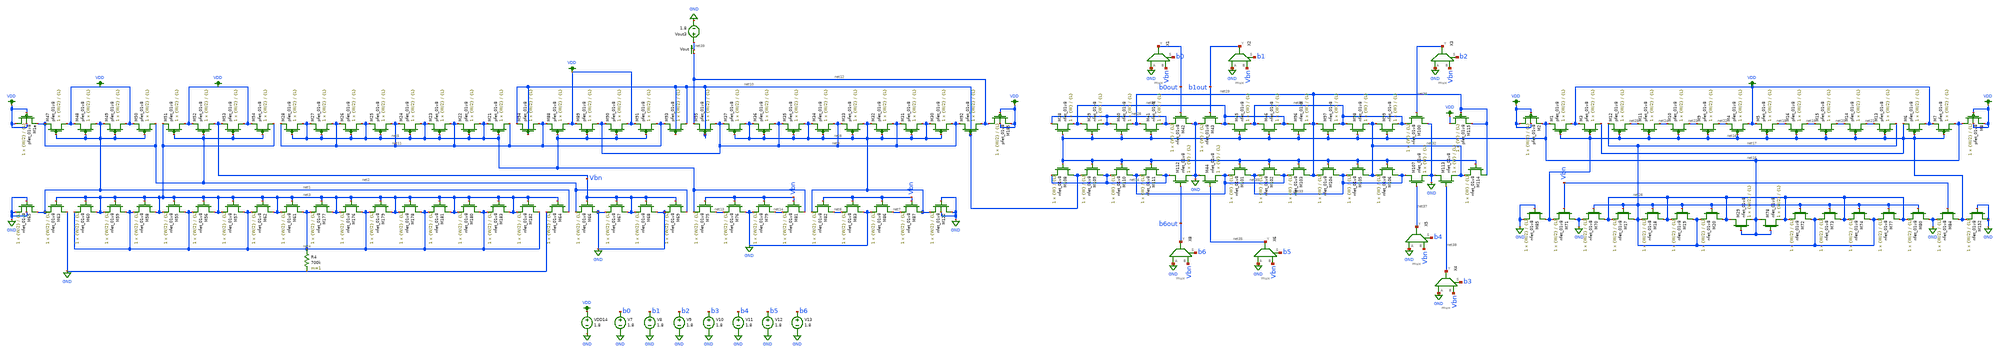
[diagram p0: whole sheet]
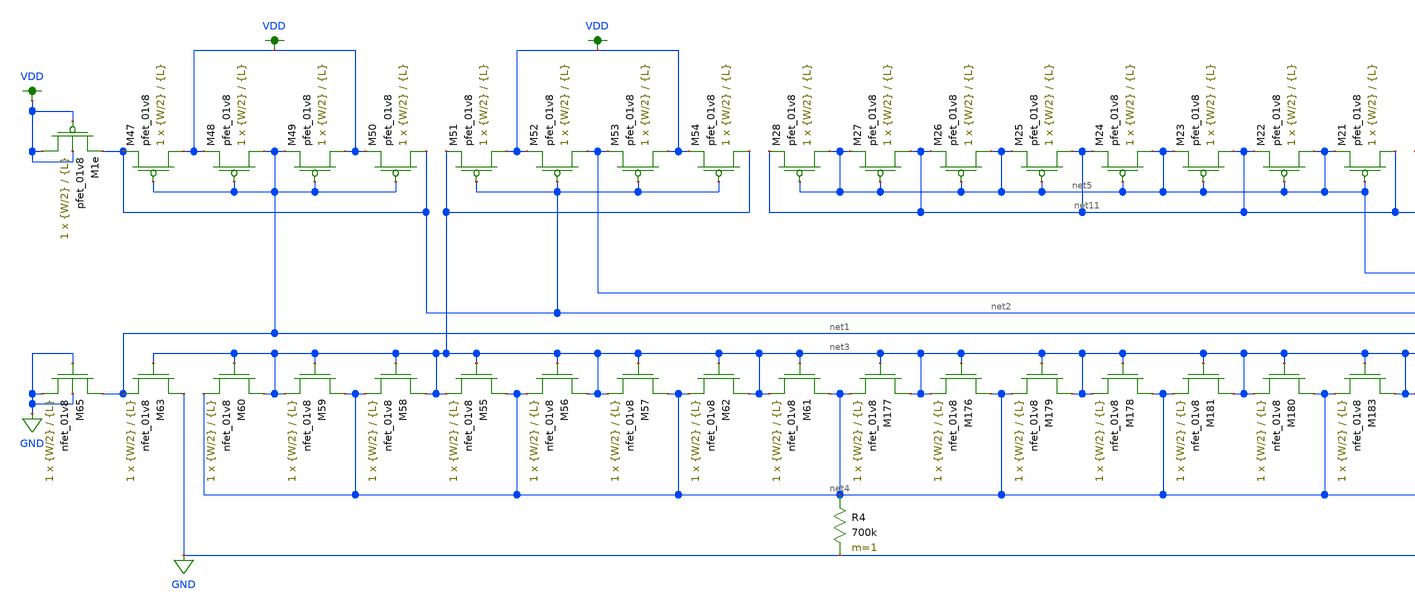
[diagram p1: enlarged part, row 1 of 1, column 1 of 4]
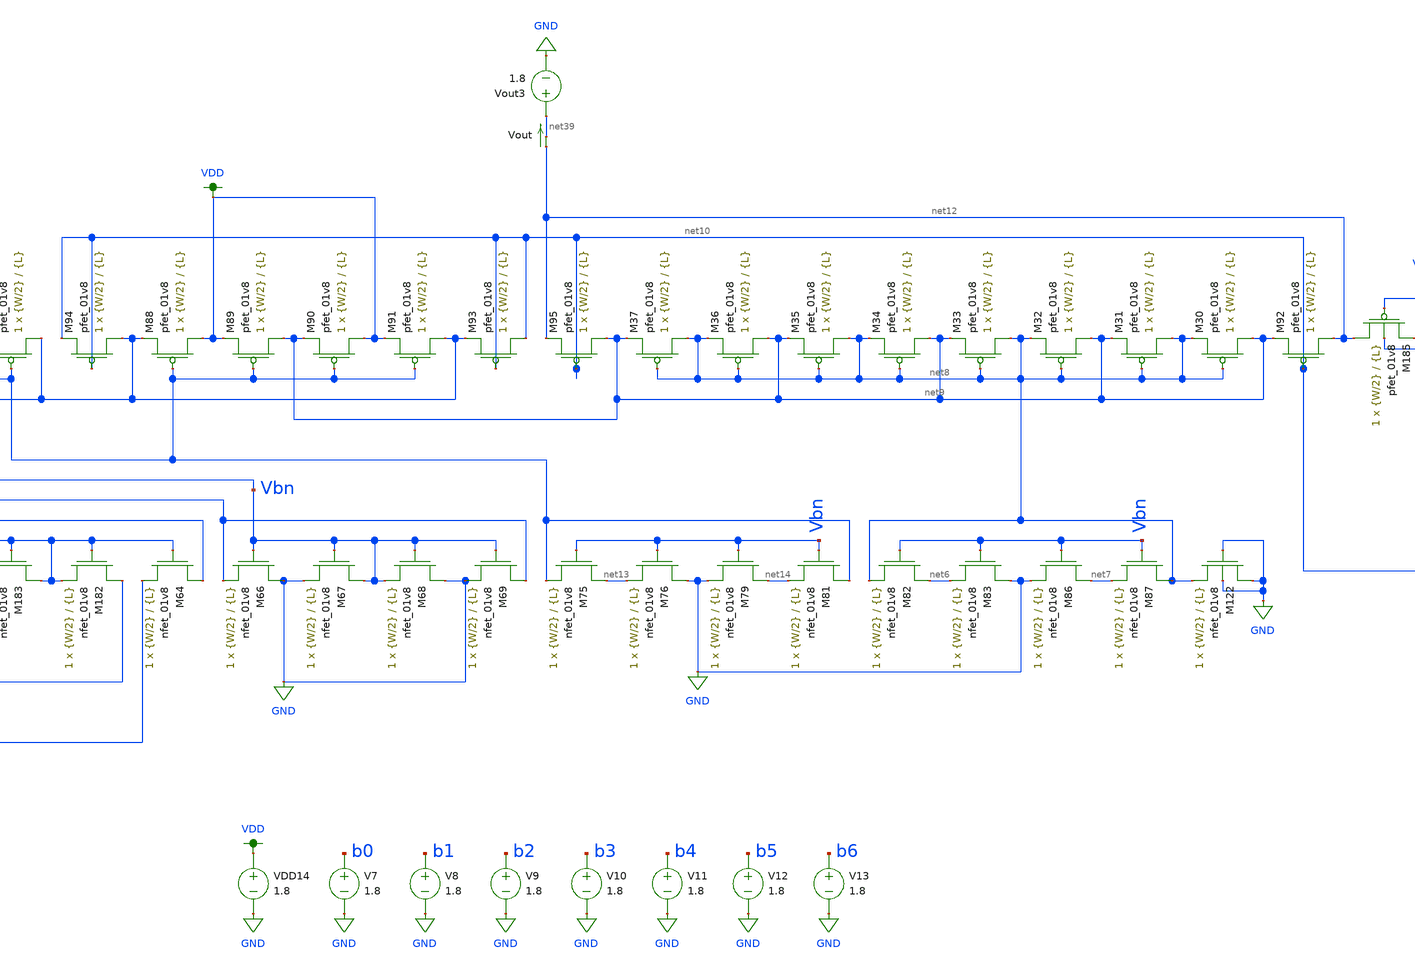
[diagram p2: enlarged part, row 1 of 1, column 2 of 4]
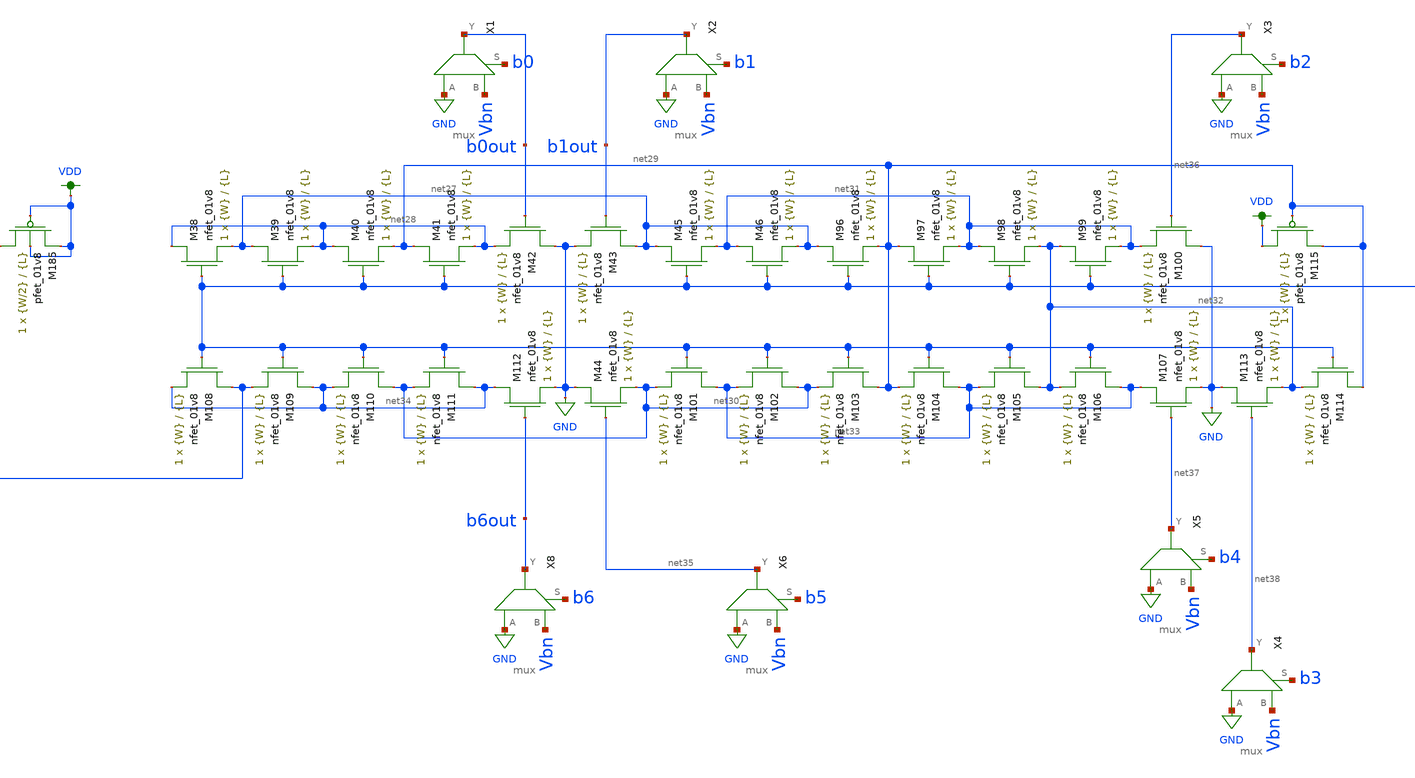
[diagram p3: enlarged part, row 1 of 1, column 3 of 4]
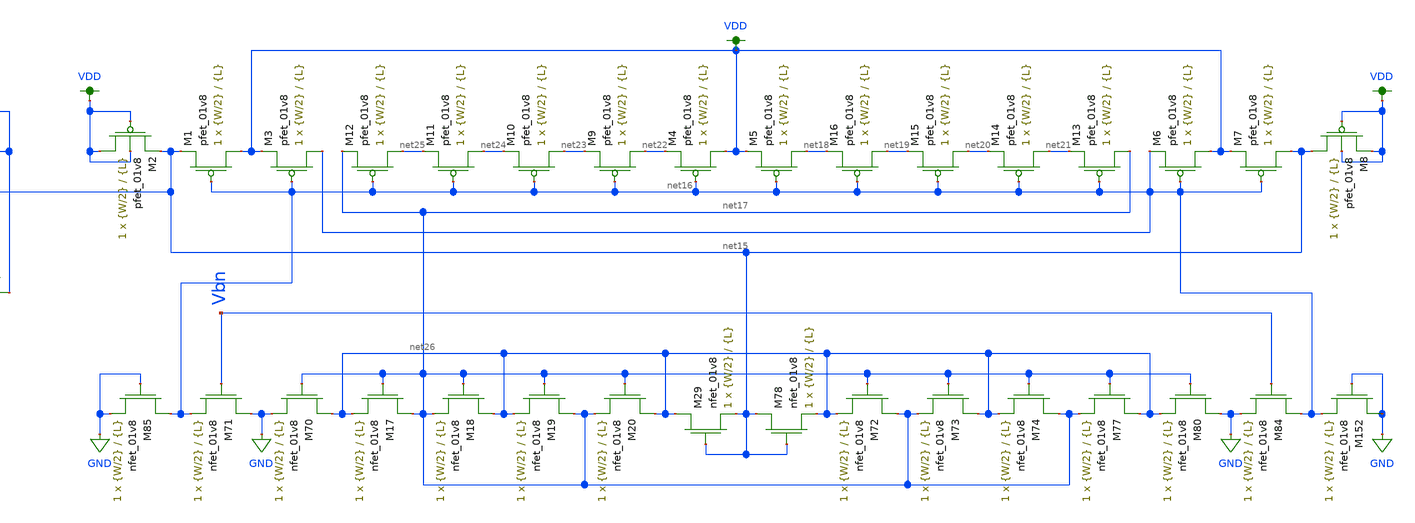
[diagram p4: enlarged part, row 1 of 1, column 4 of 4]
** sch_path: dac/schematics/dac_voltage_current_current_mirror_lds.sch
**.subckt dac_voltage_current_current_mirror_lds
XM47 VDD net1 net2 VDD sky130_fd_pr__pfet_01v8 L={L} W={W/2} nf=1 ad='int((nf+1)/2) * W/nf * 0.29' as='int((nf+2)/2) * W/nf * 0.29'
+ pd='2*int((nf+1)/2) * (W/nf + 0.29)' ps='2*int((nf+2)/2) * (W/nf + 0.29)' nrd='0.29 / W' nrs='0.29 / W'
+ sa=0 sb=0 sd=0 mult=1 m=1
XM48 net1 net1 VDD VDD sky130_fd_pr__pfet_01v8 L={L} W={W/2} nf=1 ad='int((nf+1)/2) * W/nf * 0.29' as='int((nf+2)/2) * W/nf * 0.29'
+ pd='2*int((nf+1)/2) * (W/nf + 0.29)' ps='2*int((nf+2)/2) * (W/nf + 0.29)' nrd='0.29 / W' nrs='0.29 / W'
+ sa=0 sb=0 sd=0 mult=1 m=1
XM49 VDD net1 net1 VDD sky130_fd_pr__pfet_01v8 L={L} W={W/2} nf=1 ad='int((nf+1)/2) * W/nf * 0.29' as='int((nf+2)/2) * W/nf * 0.29'
+ pd='2*int((nf+1)/2) * (W/nf + 0.29)' ps='2*int((nf+2)/2) * (W/nf + 0.29)' nrd='0.29 / W' nrs='0.29 / W'
+ sa=0 sb=0 sd=0 mult=1 m=1
XM50 net2 net1 VDD VDD sky130_fd_pr__pfet_01v8 L={L} W={W/2} nf=1 ad='int((nf+1)/2) * W/nf * 0.29' as='int((nf+2)/2) * W/nf * 0.29'
+ pd='2*int((nf+1)/2) * (W/nf + 0.29)' ps='2*int((nf+2)/2) * (W/nf + 0.29)' nrd='0.29 / W' nrs='0.29 / W'
+ sa=0 sb=0 sd=0 mult=1 m=1
XM51 VDD net2 net3 VDD sky130_fd_pr__pfet_01v8 L={L} W={W/2} nf=1 ad='int((nf+1)/2) * W/nf * 0.29' as='int((nf+2)/2) * W/nf * 0.29'
+ pd='2*int((nf+1)/2) * (W/nf + 0.29)' ps='2*int((nf+2)/2) * (W/nf + 0.29)' nrd='0.29 / W' nrs='0.29 / W'
+ sa=0 sb=0 sd=0 mult=1 m=1
XM52 Vbn net2 VDD VDD sky130_fd_pr__pfet_01v8 L={L} W={W/2} nf=1 ad='int((nf+1)/2) * W/nf * 0.29' as='int((nf+2)/2) * W/nf * 0.29'
+ pd='2*int((nf+1)/2) * (W/nf + 0.29)' ps='2*int((nf+2)/2) * (W/nf + 0.29)' nrd='0.29 / W' nrs='0.29 / W'
+ sa=0 sb=0 sd=0 mult=1 m=1
XM53 VDD net2 Vbn VDD sky130_fd_pr__pfet_01v8 L={L} W={W/2} nf=1 ad='int((nf+1)/2) * W/nf * 0.29' as='int((nf+2)/2) * W/nf * 0.29'
+ pd='2*int((nf+1)/2) * (W/nf + 0.29)' ps='2*int((nf+2)/2) * (W/nf + 0.29)' nrd='0.29 / W' nrs='0.29 / W'
+ sa=0 sb=0 sd=0 mult=1 m=1
XM54 net3 net2 VDD VDD sky130_fd_pr__pfet_01v8 L={L} W={W/2} nf=1 ad='int((nf+1)/2) * W/nf * 0.29' as='int((nf+2)/2) * W/nf * 0.29'
+ pd='2*int((nf+1)/2) * (W/nf + 0.29)' ps='2*int((nf+2)/2) * (W/nf + 0.29)' nrd='0.29 / W' nrs='0.29 / W'
+ sa=0 sb=0 sd=0 mult=1 m=1
XM55 net4 net3 net3 GND sky130_fd_pr__nfet_01v8 L={L} W={W/2} nf=1 ad='int((nf+1)/2) * W/nf * 0.29' as='int((nf+2)/2) * W/nf * 0.29'
+ pd='2*int((nf+1)/2) * (W/nf + 0.29)' ps='2*int((nf+2)/2) * (W/nf + 0.29)' nrd='0.29 / W' nrs='0.29 / W'
+ sa=0 sb=0 sd=0 mult=1 m=1
XM56 net3 net3 net4 GND sky130_fd_pr__nfet_01v8 L={L} W={W/2} nf=1 ad='int((nf+1)/2) * W/nf * 0.29' as='int((nf+2)/2) * W/nf * 0.29'
+ pd='2*int((nf+1)/2) * (W/nf + 0.29)' ps='2*int((nf+2)/2) * (W/nf + 0.29)' nrd='0.29 / W' nrs='0.29 / W'
+ sa=0 sb=0 sd=0 mult=1 m=1
XM57 net4 net3 net3 GND sky130_fd_pr__nfet_01v8 L={L} W={W/2} nf=1 ad='int((nf+1)/2) * W/nf * 0.29' as='int((nf+2)/2) * W/nf * 0.29'
+ pd='2*int((nf+1)/2) * (W/nf + 0.29)' ps='2*int((nf+2)/2) * (W/nf + 0.29)' nrd='0.29 / W' nrs='0.29 / W'
+ sa=0 sb=0 sd=0 mult=1 m=1
XM58 net3 net3 net4 GND sky130_fd_pr__nfet_01v8 L={L} W={W/2} nf=1 ad='int((nf+1)/2) * W/nf * 0.29' as='int((nf+2)/2) * W/nf * 0.29'
+ pd='2*int((nf+1)/2) * (W/nf + 0.29)' ps='2*int((nf+2)/2) * (W/nf + 0.29)' nrd='0.29 / W' nrs='0.29 / W'
+ sa=0 sb=0 sd=0 mult=1 m=1
XM59 net4 net3 net3 GND sky130_fd_pr__nfet_01v8 L={L} W={W/2} nf=1 ad='int((nf+1)/2) * W/nf * 0.29' as='int((nf+2)/2) * W/nf * 0.29'
+ pd='2*int((nf+1)/2) * (W/nf + 0.29)' ps='2*int((nf+2)/2) * (W/nf + 0.29)' nrd='0.29 / W' nrs='0.29 / W'
+ sa=0 sb=0 sd=0 mult=1 m=1
XM60 net3 net3 net4 GND sky130_fd_pr__nfet_01v8 L={L} W={W/2} nf=1 ad='int((nf+1)/2) * W/nf * 0.29' as='int((nf+2)/2) * W/nf * 0.29'
+ pd='2*int((nf+1)/2) * (W/nf + 0.29)' ps='2*int((nf+2)/2) * (W/nf + 0.29)' nrd='0.29 / W' nrs='0.29 / W'
+ sa=0 sb=0 sd=0 mult=1 m=1
XM61 net4 net3 net3 GND sky130_fd_pr__nfet_01v8 L={L} W={W/2} nf=1 ad='int((nf+1)/2) * W/nf * 0.29' as='int((nf+2)/2) * W/nf * 0.29'
+ pd='2*int((nf+1)/2) * (W/nf + 0.29)' ps='2*int((nf+2)/2) * (W/nf + 0.29)' nrd='0.29 / W' nrs='0.29 / W'
+ sa=0 sb=0 sd=0 mult=1 m=1
XM62 net3 net3 net4 GND sky130_fd_pr__nfet_01v8 L={L} W={W/2} nf=1 ad='int((nf+1)/2) * W/nf * 0.29' as='int((nf+2)/2) * W/nf * 0.29'
+ pd='2*int((nf+1)/2) * (W/nf + 0.29)' ps='2*int((nf+2)/2) * (W/nf + 0.29)' nrd='0.29 / W' nrs='0.29 / W'
+ sa=0 sb=0 sd=0 mult=1 m=1
XM63 GND net3 net1 GND sky130_fd_pr__nfet_01v8 L={L} W={W/2} nf=1 ad='int((nf+1)/2) * W/nf * 0.29' as='int((nf+2)/2) * W/nf * 0.29'
+ pd='2*int((nf+1)/2) * (W/nf + 0.29)' ps='2*int((nf+2)/2) * (W/nf + 0.29)' nrd='0.29 / W' nrs='0.29 / W'
+ sa=0 sb=0 sd=0 mult=1 m=1
XM64 net1 net3 GND GND sky130_fd_pr__nfet_01v8 L={L} W={W/2} nf=1 ad='int((nf+1)/2) * W/nf * 0.29' as='int((nf+2)/2) * W/nf * 0.29'
+ pd='2*int((nf+1)/2) * (W/nf + 0.29)' ps='2*int((nf+2)/2) * (W/nf + 0.29)' nrd='0.29 / W' nrs='0.29 / W'
+ sa=0 sb=0 sd=0 mult=1 m=1
R4 net4 GND 700k m=1
XM1e VDD VDD net2 VDD sky130_fd_pr__pfet_01v8 L={L} W={W/2} nf=1 ad='int((nf+1)/2) * W/nf * 0.29' as='int((nf+2)/2) * W/nf * 0.29'
+ pd='2*int((nf+1)/2) * (W/nf + 0.29)' ps='2*int((nf+2)/2) * (W/nf + 0.29)' nrd='0.29 / W' nrs='0.29 / W'
+ sa=0 sb=0 sd=0 mult=1 m=1
XM65 net1 GND GND GND sky130_fd_pr__nfet_01v8 L={L} W={W/2} nf=1 ad='int((nf+1)/2) * W/nf * 0.29' as='int((nf+2)/2) * W/nf * 0.29'
+ pd='2*int((nf+1)/2) * (W/nf + 0.29)' ps='2*int((nf+2)/2) * (W/nf + 0.29)' nrd='0.29 / W' nrs='0.29 / W'
+ sa=0 sb=0 sd=0 mult=1 m=1
XM66 GND Vbn net2 GND sky130_fd_pr__nfet_01v8 L={L} W={W/2} nf=1 ad='int((nf+1)/2) * W/nf * 0.29' as='int((nf+2)/2) * W/nf * 0.29'
+ pd='2*int((nf+1)/2) * (W/nf + 0.29)' ps='2*int((nf+2)/2) * (W/nf + 0.29)' nrd='0.29 / W' nrs='0.29 / W'
+ sa=0 sb=0 sd=0 mult=1 m=1
XM67 Vbn Vbn GND GND sky130_fd_pr__nfet_01v8 L={L} W={W/2} nf=1 ad='int((nf+1)/2) * W/nf * 0.29' as='int((nf+2)/2) * W/nf * 0.29'
+ pd='2*int((nf+1)/2) * (W/nf + 0.29)' ps='2*int((nf+2)/2) * (W/nf + 0.29)' nrd='0.29 / W' nrs='0.29 / W'
+ sa=0 sb=0 sd=0 mult=1 m=1
XM68 GND Vbn Vbn GND sky130_fd_pr__nfet_01v8 L={L} W={W/2} nf=1 ad='int((nf+1)/2) * W/nf * 0.29' as='int((nf+2)/2) * W/nf * 0.29'
+ pd='2*int((nf+1)/2) * (W/nf + 0.29)' ps='2*int((nf+2)/2) * (W/nf + 0.29)' nrd='0.29 / W' nrs='0.29 / W'
+ sa=0 sb=0 sd=0 mult=1 m=1
XM69 net2 Vbn GND GND sky130_fd_pr__nfet_01v8 L={L} W={W/2} nf=1 ad='int((nf+1)/2) * W/nf * 0.29' as='int((nf+2)/2) * W/nf * 0.29'
+ pd='2*int((nf+1)/2) * (W/nf + 0.29)' ps='2*int((nf+2)/2) * (W/nf + 0.29)' nrd='0.29 / W' nrs='0.29 / W'
+ sa=0 sb=0 sd=0 mult=1 m=1
XM75 net13 Vbn net5 GND sky130_fd_pr__nfet_01v8 L={L} W={W/2} nf=1 ad='int((nf+1)/2) * W/nf * 0.29' as='int((nf+2)/2) * W/nf * 0.29'
+ pd='2*int((nf+1)/2) * (W/nf + 0.29)' ps='2*int((nf+2)/2) * (W/nf + 0.29)' nrd='0.29 / W' nrs='0.29 / W'
+ sa=0 sb=0 sd=0 mult=1 m=1
XM76 GND Vbn net13 GND sky130_fd_pr__nfet_01v8 L={L} W={W/2} nf=1 ad='int((nf+1)/2) * W/nf * 0.29' as='int((nf+2)/2) * W/nf * 0.29'
+ pd='2*int((nf+1)/2) * (W/nf + 0.29)' ps='2*int((nf+2)/2) * (W/nf + 0.29)' nrd='0.29 / W' nrs='0.29 / W'
+ sa=0 sb=0 sd=0 mult=1 m=1
XM79 net14 Vbn GND GND sky130_fd_pr__nfet_01v8 L={L} W={W/2} nf=1 ad='int((nf+1)/2) * W/nf * 0.29' as='int((nf+2)/2) * W/nf * 0.29'
+ pd='2*int((nf+1)/2) * (W/nf + 0.29)' ps='2*int((nf+2)/2) * (W/nf + 0.29)' nrd='0.29 / W' nrs='0.29 / W'
+ sa=0 sb=0 sd=0 mult=1 m=1
XM81 net5 Vbn net14 GND sky130_fd_pr__nfet_01v8 L={L} W={W/2} nf=1 ad='int((nf+1)/2) * W/nf * 0.29' as='int((nf+2)/2) * W/nf * 0.29'
+ pd='2*int((nf+1)/2) * (W/nf + 0.29)' ps='2*int((nf+2)/2) * (W/nf + 0.29)' nrd='0.29 / W' nrs='0.29 / W'
+ sa=0 sb=0 sd=0 mult=1 m=1
XM82 net6 Vbn net8 GND sky130_fd_pr__nfet_01v8 L={L} W={W/2} nf=1 ad='int((nf+1)/2) * W/nf * 0.29' as='int((nf+2)/2) * W/nf * 0.29'
+ pd='2*int((nf+1)/2) * (W/nf + 0.29)' ps='2*int((nf+2)/2) * (W/nf + 0.29)' nrd='0.29 / W' nrs='0.29 / W'
+ sa=0 sb=0 sd=0 mult=1 m=1
XM83 GND Vbn net6 GND sky130_fd_pr__nfet_01v8 L={L} W={W/2} nf=1 ad='int((nf+1)/2) * W/nf * 0.29' as='int((nf+2)/2) * W/nf * 0.29'
+ pd='2*int((nf+1)/2) * (W/nf + 0.29)' ps='2*int((nf+2)/2) * (W/nf + 0.29)' nrd='0.29 / W' nrs='0.29 / W'
+ sa=0 sb=0 sd=0 mult=1 m=1
XM86 net7 Vbn GND GND sky130_fd_pr__nfet_01v8 L={L} W={W/2} nf=1 ad='int((nf+1)/2) * W/nf * 0.29' as='int((nf+2)/2) * W/nf * 0.29'
+ pd='2*int((nf+1)/2) * (W/nf + 0.29)' ps='2*int((nf+2)/2) * (W/nf + 0.29)' nrd='0.29 / W' nrs='0.29 / W'
+ sa=0 sb=0 sd=0 mult=1 m=1
XM87 net8 Vbn net7 GND sky130_fd_pr__nfet_01v8 L={L} W={W/2} nf=1 ad='int((nf+1)/2) * W/nf * 0.29' as='int((nf+2)/2) * W/nf * 0.29'
+ pd='2*int((nf+1)/2) * (W/nf + 0.29)' ps='2*int((nf+2)/2) * (W/nf + 0.29)' nrd='0.29 / W' nrs='0.29 / W'
+ sa=0 sb=0 sd=0 mult=1 m=1
XM88 VDD net5 net11 VDD sky130_fd_pr__pfet_01v8 L={L} W={W/2} nf=1 ad='int((nf+1)/2) * W/nf * 0.29' as='int((nf+2)/2) * W/nf * 0.29'
+ pd='2*int((nf+1)/2) * (W/nf + 0.29)' ps='2*int((nf+2)/2) * (W/nf + 0.29)' nrd='0.29 / W' nrs='0.29 / W'
+ sa=0 sb=0 sd=0 mult=1 m=1
XM89 net9 net5 VDD VDD sky130_fd_pr__pfet_01v8 L={L} W={W/2} nf=1 ad='int((nf+1)/2) * W/nf * 0.29' as='int((nf+2)/2) * W/nf * 0.29'
+ pd='2*int((nf+1)/2) * (W/nf + 0.29)' ps='2*int((nf+2)/2) * (W/nf + 0.29)' nrd='0.29 / W' nrs='0.29 / W'
+ sa=0 sb=0 sd=0 mult=1 m=1
XM90 VDD net5 net9 VDD sky130_fd_pr__pfet_01v8 L={L} W={W/2} nf=1 ad='int((nf+1)/2) * W/nf * 0.29' as='int((nf+2)/2) * W/nf * 0.29'
+ pd='2*int((nf+1)/2) * (W/nf + 0.29)' ps='2*int((nf+2)/2) * (W/nf + 0.29)' nrd='0.29 / W' nrs='0.29 / W'
+ sa=0 sb=0 sd=0 mult=1 m=1
XM91 net11 net5 VDD VDD sky130_fd_pr__pfet_01v8 L={L} W={W/2} nf=1 ad='int((nf+1)/2) * W/nf * 0.29' as='int((nf+2)/2) * W/nf * 0.29'
+ pd='2*int((nf+1)/2) * (W/nf + 0.29)' ps='2*int((nf+2)/2) * (W/nf + 0.29)' nrd='0.29 / W' nrs='0.29 / W'
+ sa=0 sb=0 sd=0 mult=1 m=1
XM92 net12 net10 net9 VDD sky130_fd_pr__pfet_01v8 L={L} W={W/2} nf=1 ad='int((nf+1)/2) * W/nf * 0.29'
+ as='int((nf+2)/2) * W/nf * 0.29' pd='2*int((nf+1)/2) * (W/nf + 0.29)' ps='2*int((nf+2)/2) * (W/nf + 0.29)'
+ nrd='0.29 / W' nrs='0.29 / W' sa=0 sb=0 sd=0 mult=1 m=1
XM93 net10 net10 net11 VDD sky130_fd_pr__pfet_01v8 L={L} W={W/2} nf=1 ad='int((nf+1)/2) * W/nf * 0.29'
+ as='int((nf+2)/2) * W/nf * 0.29' pd='2*int((nf+1)/2) * (W/nf + 0.29)' ps='2*int((nf+2)/2) * (W/nf + 0.29)'
+ nrd='0.29 / W' nrs='0.29 / W' sa=0 sb=0 sd=0 mult=1 m=1
XM94 net11 net10 net10 VDD sky130_fd_pr__pfet_01v8 L={L} W={W/2} nf=1 ad='int((nf+1)/2) * W/nf * 0.29'
+ as='int((nf+2)/2) * W/nf * 0.29' pd='2*int((nf+1)/2) * (W/nf + 0.29)' ps='2*int((nf+2)/2) * (W/nf + 0.29)'
+ nrd='0.29 / W' nrs='0.29 / W' sa=0 sb=0 sd=0 mult=1 m=1
XM95 net9 net10 net12 VDD sky130_fd_pr__pfet_01v8 L={L} W={W/2} nf=1 ad='int((nf+1)/2) * W/nf * 0.29'
+ as='int((nf+2)/2) * W/nf * 0.29' pd='2*int((nf+1)/2) * (W/nf + 0.29)' ps='2*int((nf+2)/2) * (W/nf + 0.29)'
+ nrd='0.29 / W' nrs='0.29 / W' sa=0 sb=0 sd=0 mult=1 m=1
XM176 net4 net3 net3 GND sky130_fd_pr__nfet_01v8 L={L} W={W/2} nf=1 ad='int((nf+1)/2) * W/nf * 0.29'
+ as='int((nf+2)/2) * W/nf * 0.29' pd='2*int((nf+1)/2) * (W/nf + 0.29)' ps='2*int((nf+2)/2) * (W/nf + 0.29)'
+ nrd='0.29 / W' nrs='0.29 / W' sa=0 sb=0 sd=0 mult=1 m=1
XM177 net3 net3 net4 GND sky130_fd_pr__nfet_01v8 L={L} W={W/2} nf=1 ad='int((nf+1)/2) * W/nf * 0.29'
+ as='int((nf+2)/2) * W/nf * 0.29' pd='2*int((nf+1)/2) * (W/nf + 0.29)' ps='2*int((nf+2)/2) * (W/nf + 0.29)'
+ nrd='0.29 / W' nrs='0.29 / W' sa=0 sb=0 sd=0 mult=1 m=1
XM178 net4 net3 net3 GND sky130_fd_pr__nfet_01v8 L={L} W={W/2} nf=1 ad='int((nf+1)/2) * W/nf * 0.29'
+ as='int((nf+2)/2) * W/nf * 0.29' pd='2*int((nf+1)/2) * (W/nf + 0.29)' ps='2*int((nf+2)/2) * (W/nf + 0.29)'
+ nrd='0.29 / W' nrs='0.29 / W' sa=0 sb=0 sd=0 mult=1 m=1
XM179 net3 net3 net4 GND sky130_fd_pr__nfet_01v8 L={L} W={W/2} nf=1 ad='int((nf+1)/2) * W/nf * 0.29'
+ as='int((nf+2)/2) * W/nf * 0.29' pd='2*int((nf+1)/2) * (W/nf + 0.29)' ps='2*int((nf+2)/2) * (W/nf + 0.29)'
+ nrd='0.29 / W' nrs='0.29 / W' sa=0 sb=0 sd=0 mult=1 m=1
XM180 net4 net3 net3 GND sky130_fd_pr__nfet_01v8 L={L} W={W/2} nf=1 ad='int((nf+1)/2) * W/nf * 0.29'
+ as='int((nf+2)/2) * W/nf * 0.29' pd='2*int((nf+1)/2) * (W/nf + 0.29)' ps='2*int((nf+2)/2) * (W/nf + 0.29)'
+ nrd='0.29 / W' nrs='0.29 / W' sa=0 sb=0 sd=0 mult=1 m=1
XM181 net3 net3 net4 GND sky130_fd_pr__nfet_01v8 L={L} W={W/2} nf=1 ad='int((nf+1)/2) * W/nf * 0.29'
+ as='int((nf+2)/2) * W/nf * 0.29' pd='2*int((nf+1)/2) * (W/nf + 0.29)' ps='2*int((nf+2)/2) * (W/nf + 0.29)'
+ nrd='0.29 / W' nrs='0.29 / W' sa=0 sb=0 sd=0 mult=1 m=1
XM182 net4 net3 net3 GND sky130_fd_pr__nfet_01v8 L={L} W={W/2} nf=1 ad='int((nf+1)/2) * W/nf * 0.29'
+ as='int((nf+2)/2) * W/nf * 0.29' pd='2*int((nf+1)/2) * (W/nf + 0.29)' ps='2*int((nf+2)/2) * (W/nf + 0.29)'
+ nrd='0.29 / W' nrs='0.29 / W' sa=0 sb=0 sd=0 mult=1 m=1
XM183 net3 net3 net4 GND sky130_fd_pr__nfet_01v8 L={L} W={W/2} nf=1 ad='int((nf+1)/2) * W/nf * 0.29'
+ as='int((nf+2)/2) * W/nf * 0.29' pd='2*int((nf+1)/2) * (W/nf + 0.29)' ps='2*int((nf+2)/2) * (W/nf + 0.29)'
+ nrd='0.29 / W' nrs='0.29 / W' sa=0 sb=0 sd=0 mult=1 m=1
XM185 net12 VDD VDD VDD sky130_fd_pr__pfet_01v8 L={L} W={W/2} nf=1 ad='int((nf+1)/2) * W/nf * 0.29' as='int((nf+2)/2) * W/nf * 0.29'
+ pd='2*int((nf+1)/2) * (W/nf + 0.29)' ps='2*int((nf+2)/2) * (W/nf + 0.29)' nrd='0.29 / W' nrs='0.29 / W'
+ sa=0 sb=0 sd=0 mult=1 m=1
Vout net12 net39 0
.save i(vout)
XM21 net11 net5 net5 VDD sky130_fd_pr__pfet_01v8 L={L} W={W/2} nf=1 ad='int((nf+1)/2) * W/nf * 0.29'
+ as='int((nf+2)/2) * W/nf * 0.29' pd='2*int((nf+1)/2) * (W/nf + 0.29)' ps='2*int((nf+2)/2) * (W/nf + 0.29)'
+ nrd='0.29 / W' nrs='0.29 / W' sa=0 sb=0 sd=0 mult=1 m=1
XM22 net5 net5 net11 VDD sky130_fd_pr__pfet_01v8 L={L} W={W/2} nf=1 ad='int((nf+1)/2) * W/nf * 0.29'
+ as='int((nf+2)/2) * W/nf * 0.29' pd='2*int((nf+1)/2) * (W/nf + 0.29)' ps='2*int((nf+2)/2) * (W/nf + 0.29)'
+ nrd='0.29 / W' nrs='0.29 / W' sa=0 sb=0 sd=0 mult=1 m=1
XM23 net11 net5 net5 VDD sky130_fd_pr__pfet_01v8 L={L} W={W/2} nf=1 ad='int((nf+1)/2) * W/nf * 0.29'
+ as='int((nf+2)/2) * W/nf * 0.29' pd='2*int((nf+1)/2) * (W/nf + 0.29)' ps='2*int((nf+2)/2) * (W/nf + 0.29)'
+ nrd='0.29 / W' nrs='0.29 / W' sa=0 sb=0 sd=0 mult=1 m=1
XM24 net5 net5 net11 VDD sky130_fd_pr__pfet_01v8 L={L} W={W/2} nf=1 ad='int((nf+1)/2) * W/nf * 0.29'
+ as='int((nf+2)/2) * W/nf * 0.29' pd='2*int((nf+1)/2) * (W/nf + 0.29)' ps='2*int((nf+2)/2) * (W/nf + 0.29)'
+ nrd='0.29 / W' nrs='0.29 / W' sa=0 sb=0 sd=0 mult=1 m=1
XM25 net11 net5 net5 VDD sky130_fd_pr__pfet_01v8 L={L} W={W/2} nf=1 ad='int((nf+1)/2) * W/nf * 0.29'
+ as='int((nf+2)/2) * W/nf * 0.29' pd='2*int((nf+1)/2) * (W/nf + 0.29)' ps='2*int((nf+2)/2) * (W/nf + 0.29)'
+ nrd='0.29 / W' nrs='0.29 / W' sa=0 sb=0 sd=0 mult=1 m=1
XM26 net5 net5 net11 VDD sky130_fd_pr__pfet_01v8 L={L} W={W/2} nf=1 ad='int((nf+1)/2) * W/nf * 0.29'
+ as='int((nf+2)/2) * W/nf * 0.29' pd='2*int((nf+1)/2) * (W/nf + 0.29)' ps='2*int((nf+2)/2) * (W/nf + 0.29)'
+ nrd='0.29 / W' nrs='0.29 / W' sa=0 sb=0 sd=0 mult=1 m=1
XM27 net11 net5 net5 VDD sky130_fd_pr__pfet_01v8 L={L} W={W/2} nf=1 ad='int((nf+1)/2) * W/nf * 0.29'
+ as='int((nf+2)/2) * W/nf * 0.29' pd='2*int((nf+1)/2) * (W/nf + 0.29)' ps='2*int((nf+2)/2) * (W/nf + 0.29)'
+ nrd='0.29 / W' nrs='0.29 / W' sa=0 sb=0 sd=0 mult=1 m=1
XM28 net5 net5 net11 VDD sky130_fd_pr__pfet_01v8 L={L} W={W/2} nf=1 ad='int((nf+1)/2) * W/nf * 0.29'
+ as='int((nf+2)/2) * W/nf * 0.29' pd='2*int((nf+1)/2) * (W/nf + 0.29)' ps='2*int((nf+2)/2) * (W/nf + 0.29)'
+ nrd='0.29 / W' nrs='0.29 / W' sa=0 sb=0 sd=0 mult=1 m=1
XM30 net9 net8 net8 VDD sky130_fd_pr__pfet_01v8 L={L} W={W/2} nf=1 ad='int((nf+1)/2) * W/nf * 0.29' as='int((nf+2)/2) * W/nf * 0.29'
+ pd='2*int((nf+1)/2) * (W/nf + 0.29)' ps='2*int((nf+2)/2) * (W/nf + 0.29)' nrd='0.29 / W' nrs='0.29 / W'
+ sa=0 sb=0 sd=0 mult=1 m=1
XM31 net8 net8 net9 VDD sky130_fd_pr__pfet_01v8 L={L} W={W/2} nf=1 ad='int((nf+1)/2) * W/nf * 0.29' as='int((nf+2)/2) * W/nf * 0.29'
+ pd='2*int((nf+1)/2) * (W/nf + 0.29)' ps='2*int((nf+2)/2) * (W/nf + 0.29)' nrd='0.29 / W' nrs='0.29 / W'
+ sa=0 sb=0 sd=0 mult=1 m=1
XM32 net9 net8 net8 VDD sky130_fd_pr__pfet_01v8 L={L} W={W/2} nf=1 ad='int((nf+1)/2) * W/nf * 0.29' as='int((nf+2)/2) * W/nf * 0.29'
+ pd='2*int((nf+1)/2) * (W/nf + 0.29)' ps='2*int((nf+2)/2) * (W/nf + 0.29)' nrd='0.29 / W' nrs='0.29 / W'
+ sa=0 sb=0 sd=0 mult=1 m=1
XM33 net8 net8 net9 VDD sky130_fd_pr__pfet_01v8 L={L} W={W/2} nf=1 ad='int((nf+1)/2) * W/nf * 0.29' as='int((nf+2)/2) * W/nf * 0.29'
+ pd='2*int((nf+1)/2) * (W/nf + 0.29)' ps='2*int((nf+2)/2) * (W/nf + 0.29)' nrd='0.29 / W' nrs='0.29 / W'
+ sa=0 sb=0 sd=0 mult=1 m=1
XM34 net9 net8 net8 VDD sky130_fd_pr__pfet_01v8 L={L} W={W/2} nf=1 ad='int((nf+1)/2) * W/nf * 0.29' as='int((nf+2)/2) * W/nf * 0.29'
+ pd='2*int((nf+1)/2) * (W/nf + 0.29)' ps='2*int((nf+2)/2) * (W/nf + 0.29)' nrd='0.29 / W' nrs='0.29 / W'
+ sa=0 sb=0 sd=0 mult=1 m=1
XM35 net8 net8 net9 VDD sky130_fd_pr__pfet_01v8 L={L} W={W/2} nf=1 ad='int((nf+1)/2) * W/nf * 0.29' as='int((nf+2)/2) * W/nf * 0.29'
+ pd='2*int((nf+1)/2) * (W/nf + 0.29)' ps='2*int((nf+2)/2) * (W/nf + 0.29)' nrd='0.29 / W' nrs='0.29 / W'
+ sa=0 sb=0 sd=0 mult=1 m=1
XM36 net9 net8 net8 VDD sky130_fd_pr__pfet_01v8 L={L} W={W/2} nf=1 ad='int((nf+1)/2) * W/nf * 0.29' as='int((nf+2)/2) * W/nf * 0.29'
+ pd='2*int((nf+1)/2) * (W/nf + 0.29)' ps='2*int((nf+2)/2) * (W/nf + 0.29)' nrd='0.29 / W' nrs='0.29 / W'
+ sa=0 sb=0 sd=0 mult=1 m=1
XM37 net8 net8 net9 VDD sky130_fd_pr__pfet_01v8 L={L} W={W/2} nf=1 ad='int((nf+1)/2) * W/nf * 0.29' as='int((nf+2)/2) * W/nf * 0.29'
+ pd='2*int((nf+1)/2) * (W/nf + 0.29)' ps='2*int((nf+2)/2) * (W/nf + 0.29)' nrd='0.29 / W' nrs='0.29 / W'
+ sa=0 sb=0 sd=0 mult=1 m=1
XM122 GND GND net8 GND sky130_fd_pr__nfet_01v8 L={L} W={W/2} nf=1 ad='int((nf+1)/2) * W/nf * 0.29' as='int((nf+2)/2) * W/nf * 0.29'
+ pd='2*int((nf+1)/2) * (W/nf + 0.29)' ps='2*int((nf+2)/2) * (W/nf + 0.29)' nrd='0.29 / W' nrs='0.29 / W'
+ sa=0 sb=0 sd=0 mult=1 m=1
XM1 VDD net16 net15 VDD sky130_fd_pr__pfet_01v8 L={L} W={W/2} nf=1 ad='int((nf+1)/2) * W/nf * 0.29' as='int((nf+2)/2) * W/nf * 0.29'
+ pd='2*int((nf+1)/2) * (W/nf + 0.29)' ps='2*int((nf+2)/2) * (W/nf + 0.29)' nrd='0.29 / W' nrs='0.29 / W'
+ sa=0 sb=0 sd=0 mult=1 m=1
XM2 VDD VDD net15 VDD sky130_fd_pr__pfet_01v8 L={L} W={W/2} nf=1 ad='int((nf+1)/2) * W/nf * 0.29' as='int((nf+2)/2) * W/nf * 0.29'
+ pd='2*int((nf+1)/2) * (W/nf + 0.29)' ps='2*int((nf+2)/2) * (W/nf + 0.29)' nrd='0.29 / W' nrs='0.29 / W'
+ sa=0 sb=0 sd=0 mult=1 m=1
XM3 net16 net16 VDD VDD sky130_fd_pr__pfet_01v8 L={L} W={W/2} nf=1 ad='int((nf+1)/2) * W/nf * 0.29' as='int((nf+2)/2) * W/nf * 0.29'
+ pd='2*int((nf+1)/2) * (W/nf + 0.29)' ps='2*int((nf+2)/2) * (W/nf + 0.29)' nrd='0.29 / W' nrs='0.29 / W'
+ sa=0 sb=0 sd=0 mult=1 m=1
XM4 VDD net16 net22 VDD sky130_fd_pr__pfet_01v8 L={L} W={W/2} nf=1 ad='int((nf+1)/2) * W/nf * 0.29' as='int((nf+2)/2) * W/nf * 0.29'
+ pd='2*int((nf+1)/2) * (W/nf + 0.29)' ps='2*int((nf+2)/2) * (W/nf + 0.29)' nrd='0.29 / W' nrs='0.29 / W'
+ sa=0 sb=0 sd=0 mult=1 m=1
XM5 net18 net16 VDD VDD sky130_fd_pr__pfet_01v8 L={L} W={W/2} nf=1 ad='int((nf+1)/2) * W/nf * 0.29' as='int((nf+2)/2) * W/nf * 0.29'
+ pd='2*int((nf+1)/2) * (W/nf + 0.29)' ps='2*int((nf+2)/2) * (W/nf + 0.29)' nrd='0.29 / W' nrs='0.29 / W'
+ sa=0 sb=0 sd=0 mult=1 m=1
XM6 VDD net16 net16 VDD sky130_fd_pr__pfet_01v8 L={L} W={W/2} nf=1 ad='int((nf+1)/2) * W/nf * 0.29' as='int((nf+2)/2) * W/nf * 0.29'
+ pd='2*int((nf+1)/2) * (W/nf + 0.29)' ps='2*int((nf+2)/2) * (W/nf + 0.29)' nrd='0.29 / W' nrs='0.29 / W'
+ sa=0 sb=0 sd=0 mult=1 m=1
XM7 net15 net16 VDD VDD sky130_fd_pr__pfet_01v8 L={L} W={W/2} nf=1 ad='int((nf+1)/2) * W/nf * 0.29' as='int((nf+2)/2) * W/nf * 0.29'
+ pd='2*int((nf+1)/2) * (W/nf + 0.29)' ps='2*int((nf+2)/2) * (W/nf + 0.29)' nrd='0.29 / W' nrs='0.29 / W'
+ sa=0 sb=0 sd=0 mult=1 m=1
XM8 net15 VDD VDD VDD sky130_fd_pr__pfet_01v8 L={L} W={W/2} nf=1 ad='int((nf+1)/2) * W/nf * 0.29' as='int((nf+2)/2) * W/nf * 0.29'
+ pd='2*int((nf+1)/2) * (W/nf + 0.29)' ps='2*int((nf+2)/2) * (W/nf + 0.29)' nrd='0.29 / W' nrs='0.29 / W'
+ sa=0 sb=0 sd=0 mult=1 m=1
XM9 net22 net16 net23 VDD sky130_fd_pr__pfet_01v8 L={L} W={W/2} nf=1 ad='int((nf+1)/2) * W/nf * 0.29'
+ as='int((nf+2)/2) * W/nf * 0.29' pd='2*int((nf+1)/2) * (W/nf + 0.29)' ps='2*int((nf+2)/2) * (W/nf + 0.29)'
+ nrd='0.29 / W' nrs='0.29 / W' sa=0 sb=0 sd=0 mult=1 m=1
XM10 net23 net16 net24 VDD sky130_fd_pr__pfet_01v8 L={L} W={W/2} nf=1 ad='int((nf+1)/2) * W/nf * 0.29'
+ as='int((nf+2)/2) * W/nf * 0.29' pd='2*int((nf+1)/2) * (W/nf + 0.29)' ps='2*int((nf+2)/2) * (W/nf + 0.29)'
+ nrd='0.29 / W' nrs='0.29 / W' sa=0 sb=0 sd=0 mult=1 m=1
XM11 net24 net16 net25 VDD sky130_fd_pr__pfet_01v8 L={L} W={W/2} nf=1 ad='int((nf+1)/2) * W/nf * 0.29'
+ as='int((nf+2)/2) * W/nf * 0.29' pd='2*int((nf+1)/2) * (W/nf + 0.29)' ps='2*int((nf+2)/2) * (W/nf + 0.29)'
+ nrd='0.29 / W' nrs='0.29 / W' sa=0 sb=0 sd=0 mult=1 m=1
XM12 net25 net16 net17 VDD sky130_fd_pr__pfet_01v8 L={L} W={W/2} nf=1 ad='int((nf+1)/2) * W/nf * 0.29'
+ as='int((nf+2)/2) * W/nf * 0.29' pd='2*int((nf+1)/2) * (W/nf + 0.29)' ps='2*int((nf+2)/2) * (W/nf + 0.29)'
+ nrd='0.29 / W' nrs='0.29 / W' sa=0 sb=0 sd=0 mult=1 m=1
XM13 net17 net16 net21 VDD sky130_fd_pr__pfet_01v8 L={L} W={W/2} nf=1 ad='int((nf+1)/2) * W/nf * 0.29'
+ as='int((nf+2)/2) * W/nf * 0.29' pd='2*int((nf+1)/2) * (W/nf + 0.29)' ps='2*int((nf+2)/2) * (W/nf + 0.29)'
+ nrd='0.29 / W' nrs='0.29 / W' sa=0 sb=0 sd=0 mult=1 m=1
XM14 net21 net16 net20 VDD sky130_fd_pr__pfet_01v8 L={L} W={W/2} nf=1 ad='int((nf+1)/2) * W/nf * 0.29'
+ as='int((nf+2)/2) * W/nf * 0.29' pd='2*int((nf+1)/2) * (W/nf + 0.29)' ps='2*int((nf+2)/2) * (W/nf + 0.29)'
+ nrd='0.29 / W' nrs='0.29 / W' sa=0 sb=0 sd=0 mult=1 m=1
XM15 net20 net16 net19 VDD sky130_fd_pr__pfet_01v8 L={L} W={W/2} nf=1 ad='int((nf+1)/2) * W/nf * 0.29'
+ as='int((nf+2)/2) * W/nf * 0.29' pd='2*int((nf+1)/2) * (W/nf + 0.29)' ps='2*int((nf+2)/2) * (W/nf + 0.29)'
+ nrd='0.29 / W' nrs='0.29 / W' sa=0 sb=0 sd=0 mult=1 m=1
XM16 net19 net16 net18 VDD sky130_fd_pr__pfet_01v8 L={L} W={W/2} nf=1 ad='int((nf+1)/2) * W/nf * 0.29'
+ as='int((nf+2)/2) * W/nf * 0.29' pd='2*int((nf+1)/2) * (W/nf + 0.29)' ps='2*int((nf+2)/2) * (W/nf + 0.29)'
+ nrd='0.29 / W' nrs='0.29 / W' sa=0 sb=0 sd=0 mult=1 m=1
XM17 net17 net17 net26 GND sky130_fd_pr__nfet_01v8 L={L} W={W/2} nf=1 ad='int((nf+1)/2) * W/nf * 0.29'
+ as='int((nf+2)/2) * W/nf * 0.29' pd='2*int((nf+1)/2) * (W/nf + 0.29)' ps='2*int((nf+2)/2) * (W/nf + 0.29)'
+ nrd='0.29 / W' nrs='0.29 / W' sa=0 sb=0 sd=0 mult=1 m=1
XM18 net26 net17 net17 GND sky130_fd_pr__nfet_01v8 L={L} W={W/2} nf=1 ad='int((nf+1)/2) * W/nf * 0.29'
+ as='int((nf+2)/2) * W/nf * 0.29' pd='2*int((nf+1)/2) * (W/nf + 0.29)' ps='2*int((nf+2)/2) * (W/nf + 0.29)'
+ nrd='0.29 / W' nrs='0.29 / W' sa=0 sb=0 sd=0 mult=1 m=1
XM19 net17 net17 net26 GND sky130_fd_pr__nfet_01v8 L={L} W={W/2} nf=1 ad='int((nf+1)/2) * W/nf * 0.29'
+ as='int((nf+2)/2) * W/nf * 0.29' pd='2*int((nf+1)/2) * (W/nf + 0.29)' ps='2*int((nf+2)/2) * (W/nf + 0.29)'
+ nrd='0.29 / W' nrs='0.29 / W' sa=0 sb=0 sd=0 mult=1 m=1
XM20 net26 net17 net17 GND sky130_fd_pr__nfet_01v8 L={L} W={W/2} nf=1 ad='int((nf+1)/2) * W/nf * 0.29'
+ as='int((nf+2)/2) * W/nf * 0.29' pd='2*int((nf+1)/2) * (W/nf + 0.29)' ps='2*int((nf+2)/2) * (W/nf + 0.29)'
+ nrd='0.29 / W' nrs='0.29 / W' sa=0 sb=0 sd=0 mult=1 m=1
XM29 net26 net15 net15 GND sky130_fd_pr__nfet_01v8 L={L} W={W/2} nf=1 ad='int((nf+1)/2) * W/nf * 0.29'
+ as='int((nf+2)/2) * W/nf * 0.29' pd='2*int((nf+1)/2) * (W/nf + 0.29)' ps='2*int((nf+2)/2) * (W/nf + 0.29)'
+ nrd='0.29 / W' nrs='0.29 / W' sa=0 sb=0 sd=0 mult=1 m=1
XM70 net26 net17 GND GND sky130_fd_pr__nfet_01v8 L={L} W={W/2} nf=1 ad='int((nf+1)/2) * W/nf * 0.29'
+ as='int((nf+2)/2) * W/nf * 0.29' pd='2*int((nf+1)/2) * (W/nf + 0.29)' ps='2*int((nf+2)/2) * (W/nf + 0.29)'
+ nrd='0.29 / W' nrs='0.29 / W' sa=0 sb=0 sd=0 mult=1 m=1
XM71 GND Vbn net16 GND sky130_fd_pr__nfet_01v8 L={L} W={W/2} nf=1 ad='int((nf+1)/2) * W/nf * 0.29' as='int((nf+2)/2) * W/nf * 0.29'
+ pd='2*int((nf+1)/2) * (W/nf + 0.29)' ps='2*int((nf+2)/2) * (W/nf + 0.29)' nrd='0.29 / W' nrs='0.29 / W'
+ sa=0 sb=0 sd=0 mult=1 m=1
XM72 net17 net17 net26 GND sky130_fd_pr__nfet_01v8 L={L} W={W/2} nf=1 ad='int((nf+1)/2) * W/nf * 0.29'
+ as='int((nf+2)/2) * W/nf * 0.29' pd='2*int((nf+1)/2) * (W/nf + 0.29)' ps='2*int((nf+2)/2) * (W/nf + 0.29)'
+ nrd='0.29 / W' nrs='0.29 / W' sa=0 sb=0 sd=0 mult=1 m=1
XM73 net26 net17 net17 GND sky130_fd_pr__nfet_01v8 L={L} W={W/2} nf=1 ad='int((nf+1)/2) * W/nf * 0.29'
+ as='int((nf+2)/2) * W/nf * 0.29' pd='2*int((nf+1)/2) * (W/nf + 0.29)' ps='2*int((nf+2)/2) * (W/nf + 0.29)'
+ nrd='0.29 / W' nrs='0.29 / W' sa=0 sb=0 sd=0 mult=1 m=1
XM74 net17 net17 net26 GND sky130_fd_pr__nfet_01v8 L={L} W={W/2} nf=1 ad='int((nf+1)/2) * W/nf * 0.29'
+ as='int((nf+2)/2) * W/nf * 0.29' pd='2*int((nf+1)/2) * (W/nf + 0.29)' ps='2*int((nf+2)/2) * (W/nf + 0.29)'
+ nrd='0.29 / W' nrs='0.29 / W' sa=0 sb=0 sd=0 mult=1 m=1
XM77 net26 net17 net17 GND sky130_fd_pr__nfet_01v8 L={L} W={W/2} nf=1 ad='int((nf+1)/2) * W/nf * 0.29'
+ as='int((nf+2)/2) * W/nf * 0.29' pd='2*int((nf+1)/2) * (W/nf + 0.29)' ps='2*int((nf+2)/2) * (W/nf + 0.29)'
+ nrd='0.29 / W' nrs='0.29 / W' sa=0 sb=0 sd=0 mult=1 m=1
XM78 net15 net15 net26 GND sky130_fd_pr__nfet_01v8 L={L} W={W/2} nf=1 ad='int((nf+1)/2) * W/nf * 0.29'
+ as='int((nf+2)/2) * W/nf * 0.29' pd='2*int((nf+1)/2) * (W/nf + 0.29)' ps='2*int((nf+2)/2) * (W/nf + 0.29)'
+ nrd='0.29 / W' nrs='0.29 / W' sa=0 sb=0 sd=0 mult=1 m=1
XM80 GND net17 net26 GND sky130_fd_pr__nfet_01v8 L={L} W={W/2} nf=1 ad='int((nf+1)/2) * W/nf * 0.29'
+ as='int((nf+2)/2) * W/nf * 0.29' pd='2*int((nf+1)/2) * (W/nf + 0.29)' ps='2*int((nf+2)/2) * (W/nf + 0.29)'
+ nrd='0.29 / W' nrs='0.29 / W' sa=0 sb=0 sd=0 mult=1 m=1
XM84 net16 Vbn GND GND sky130_fd_pr__nfet_01v8 L={L} W={W/2} nf=1 ad='int((nf+1)/2) * W/nf * 0.29' as='int((nf+2)/2) * W/nf * 0.29'
+ pd='2*int((nf+1)/2) * (W/nf + 0.29)' ps='2*int((nf+2)/2) * (W/nf + 0.29)' nrd='0.29 / W' nrs='0.29 / W'
+ sa=0 sb=0 sd=0 mult=1 m=1
XM85 net16 GND GND GND sky130_fd_pr__nfet_01v8 L={L} W={W/2} nf=1 ad='int((nf+1)/2) * W/nf * 0.29' as='int((nf+2)/2) * W/nf * 0.29'
+ pd='2*int((nf+1)/2) * (W/nf + 0.29)' ps='2*int((nf+2)/2) * (W/nf + 0.29)' nrd='0.29 / W' nrs='0.29 / W'
+ sa=0 sb=0 sd=0 mult=1 m=1
XM152 GND GND net16 GND sky130_fd_pr__nfet_01v8 L={L} W={W/2} nf=1 ad='int((nf+1)/2) * W/nf * 0.29' as='int((nf+2)/2) * W/nf * 0.29'
+ pd='2*int((nf+1)/2) * (W/nf + 0.29)' ps='2*int((nf+2)/2) * (W/nf + 0.29)' nrd='0.29 / W' nrs='0.29 / W'
+ sa=0 sb=0 sd=0 mult=1 m=1
X1 GND Vbn b0out b0 mux
X2 GND Vbn b1out b1 mux
X3 GND Vbn net36 b2 mux
X4 GND Vbn net38 b3 mux
X5 GND Vbn net37 b4 mux
X6 GND Vbn net35 b5 mux
X8 GND Vbn b6out b6 mux
XM38 net28 net15 net27 GND sky130_fd_pr__nfet_01v8 L={L} W={W} nf=1 ad='int((nf+1)/2) * W/nf * 0.29'
+ as='int((nf+2)/2) * W/nf * 0.29' pd='2*int((nf+1)/2) * (W/nf + 0.29)' ps='2*int((nf+2)/2) * (W/nf + 0.29)'
+ nrd='0.29 / W' nrs='0.29 / W' sa=0 sb=0 sd=0 mult=1 m=1
XM39 net27 net15 net28 GND sky130_fd_pr__nfet_01v8 L={L} W={W} nf=1 ad='int((nf+1)/2) * W/nf * 0.29'
+ as='int((nf+2)/2) * W/nf * 0.29' pd='2*int((nf+1)/2) * (W/nf + 0.29)' ps='2*int((nf+2)/2) * (W/nf + 0.29)'
+ nrd='0.29 / W' nrs='0.29 / W' sa=0 sb=0 sd=0 mult=1 m=1
XM40 net28 net15 net29 GND sky130_fd_pr__nfet_01v8 L={L} W={W} nf=1 ad='int((nf+1)/2) * W/nf * 0.29'
+ as='int((nf+2)/2) * W/nf * 0.29' pd='2*int((nf+1)/2) * (W/nf + 0.29)' ps='2*int((nf+2)/2) * (W/nf + 0.29)'
+ nrd='0.29 / W' nrs='0.29 / W' sa=0 sb=0 sd=0 mult=1 m=1
XM41 net29 net15 net28 GND sky130_fd_pr__nfet_01v8 L={L} W={W} nf=1 ad='int((nf+1)/2) * W/nf * 0.29'
+ as='int((nf+2)/2) * W/nf * 0.29' pd='2*int((nf+1)/2) * (W/nf + 0.29)' ps='2*int((nf+2)/2) * (W/nf + 0.29)'
+ nrd='0.29 / W' nrs='0.29 / W' sa=0 sb=0 sd=0 mult=1 m=1
XM42 GND b0out net28 GND sky130_fd_pr__nfet_01v8 L={L} W={W} nf=1 ad='int((nf+1)/2) * W/nf * 0.29' as='int((nf+2)/2) * W/nf * 0.29'
+ pd='2*int((nf+1)/2) * (W/nf + 0.29)' ps='2*int((nf+2)/2) * (W/nf + 0.29)' nrd='0.29 / W' nrs='0.29 / W'
+ sa=0 sb=0 sd=0 mult=1 m=1
XM43 net27 b1out GND GND sky130_fd_pr__nfet_01v8 L={L} W={W} nf=1 ad='int((nf+1)/2) * W/nf * 0.29' as='int((nf+2)/2) * W/nf * 0.29'
+ pd='2*int((nf+1)/2) * (W/nf + 0.29)' ps='2*int((nf+2)/2) * (W/nf + 0.29)' nrd='0.29 / W' nrs='0.29 / W'
+ sa=0 sb=0 sd=0 mult=1 m=1
XM44 GND net35 net30 GND sky130_fd_pr__nfet_01v8 L={L} W={W} nf=1 ad='int((nf+1)/2) * W/nf * 0.29' as='int((nf+2)/2) * W/nf * 0.29'
+ pd='2*int((nf+1)/2) * (W/nf + 0.29)' ps='2*int((nf+2)/2) * (W/nf + 0.29)' nrd='0.29 / W' nrs='0.29 / W'
+ sa=0 sb=0 sd=0 mult=1 m=1
XM45 net27 net15 net31 GND sky130_fd_pr__nfet_01v8 L={L} W={W} nf=1 ad='int((nf+1)/2) * W/nf * 0.29'
+ as='int((nf+2)/2) * W/nf * 0.29' pd='2*int((nf+1)/2) * (W/nf + 0.29)' ps='2*int((nf+2)/2) * (W/nf + 0.29)'
+ nrd='0.29 / W' nrs='0.29 / W' sa=0 sb=0 sd=0 mult=1 m=1
XM46 net31 net15 net27 GND sky130_fd_pr__nfet_01v8 L={L} W={W} nf=1 ad='int((nf+1)/2) * W/nf * 0.29'
+ as='int((nf+2)/2) * W/nf * 0.29' pd='2*int((nf+1)/2) * (W/nf + 0.29)' ps='2*int((nf+2)/2) * (W/nf + 0.29)'
+ nrd='0.29 / W' nrs='0.29 / W' sa=0 sb=0 sd=0 mult=1 m=1
XM96 net27 net15 net29 GND sky130_fd_pr__nfet_01v8 L={L} W={W} nf=1 ad='int((nf+1)/2) * W/nf * 0.29'
+ as='int((nf+2)/2) * W/nf * 0.29' pd='2*int((nf+1)/2) * (W/nf + 0.29)' ps='2*int((nf+2)/2) * (W/nf + 0.29)'
+ nrd='0.29 / W' nrs='0.29 / W' sa=0 sb=0 sd=0 mult=1 m=1
XM97 net29 net15 net31 GND sky130_fd_pr__nfet_01v8 L={L} W={W} nf=1 ad='int((nf+1)/2) * W/nf * 0.29'
+ as='int((nf+2)/2) * W/nf * 0.29' pd='2*int((nf+1)/2) * (W/nf + 0.29)' ps='2*int((nf+2)/2) * (W/nf + 0.29)'
+ nrd='0.29 / W' nrs='0.29 / W' sa=0 sb=0 sd=0 mult=1 m=1
XM98 net31 net15 net32 GND sky130_fd_pr__nfet_01v8 L={L} W={W} nf=1 ad='int((nf+1)/2) * W/nf * 0.29'
+ as='int((nf+2)/2) * W/nf * 0.29' pd='2*int((nf+1)/2) * (W/nf + 0.29)' ps='2*int((nf+2)/2) * (W/nf + 0.29)'
+ nrd='0.29 / W' nrs='0.29 / W' sa=0 sb=0 sd=0 mult=1 m=1
XM99 net32 net15 net31 GND sky130_fd_pr__nfet_01v8 L={L} W={W} nf=1 ad='int((nf+1)/2) * W/nf * 0.29'
+ as='int((nf+2)/2) * W/nf * 0.29' pd='2*int((nf+1)/2) * (W/nf + 0.29)' ps='2*int((nf+2)/2) * (W/nf + 0.29)'
+ nrd='0.29 / W' nrs='0.29 / W' sa=0 sb=0 sd=0 mult=1 m=1
XM100 GND net36 net31 GND sky130_fd_pr__nfet_01v8 L={L} W={W} nf=1 ad='int((nf+1)/2) * W/nf * 0.29' as='int((nf+2)/2) * W/nf * 0.29'
+ pd='2*int((nf+1)/2) * (W/nf + 0.29)' ps='2*int((nf+2)/2) * (W/nf + 0.29)' nrd='0.29 / W' nrs='0.29 / W'
+ sa=0 sb=0 sd=0 mult=1 m=1
XM101 net33 net15 net30 GND sky130_fd_pr__nfet_01v8 L={L} W={W} nf=1 ad='int((nf+1)/2) * W/nf * 0.29'
+ as='int((nf+2)/2) * W/nf * 0.29' pd='2*int((nf+1)/2) * (W/nf + 0.29)' ps='2*int((nf+2)/2) * (W/nf + 0.29)'
+ nrd='0.29 / W' nrs='0.29 / W' sa=0 sb=0 sd=0 mult=1 m=1
XM102 net30 net15 net33 GND sky130_fd_pr__nfet_01v8 L={L} W={W} nf=1 ad='int((nf+1)/2) * W/nf * 0.29'
+ as='int((nf+2)/2) * W/nf * 0.29' pd='2*int((nf+1)/2) * (W/nf + 0.29)' ps='2*int((nf+2)/2) * (W/nf + 0.29)'
+ nrd='0.29 / W' nrs='0.29 / W' sa=0 sb=0 sd=0 mult=1 m=1
XM103 net29 net15 net30 GND sky130_fd_pr__nfet_01v8 L={L} W={W} nf=1 ad='int((nf+1)/2) * W/nf * 0.29'
+ as='int((nf+2)/2) * W/nf * 0.29' pd='2*int((nf+1)/2) * (W/nf + 0.29)' ps='2*int((nf+2)/2) * (W/nf + 0.29)'
+ nrd='0.29 / W' nrs='0.29 / W' sa=0 sb=0 sd=0 mult=1 m=1
XM104 net33 net15 net29 GND sky130_fd_pr__nfet_01v8 L={L} W={W} nf=1 ad='int((nf+1)/2) * W/nf * 0.29'
+ as='int((nf+2)/2) * W/nf * 0.29' pd='2*int((nf+1)/2) * (W/nf + 0.29)' ps='2*int((nf+2)/2) * (W/nf + 0.29)'
+ nrd='0.29 / W' nrs='0.29 / W' sa=0 sb=0 sd=0 mult=1 m=1
XM105 net32 net15 net33 GND sky130_fd_pr__nfet_01v8 L={L} W={W} nf=1 ad='int((nf+1)/2) * W/nf * 0.29'
+ as='int((nf+2)/2) * W/nf * 0.29' pd='2*int((nf+1)/2) * (W/nf + 0.29)' ps='2*int((nf+2)/2) * (W/nf + 0.29)'
+ nrd='0.29 / W' nrs='0.29 / W' sa=0 sb=0 sd=0 mult=1 m=1
XM106 net33 net15 net32 GND sky130_fd_pr__nfet_01v8 L={L} W={W} nf=1 ad='int((nf+1)/2) * W/nf * 0.29'
+ as='int((nf+2)/2) * W/nf * 0.29' pd='2*int((nf+1)/2) * (W/nf + 0.29)' ps='2*int((nf+2)/2) * (W/nf + 0.29)'
+ nrd='0.29 / W' nrs='0.29 / W' sa=0 sb=0 sd=0 mult=1 m=1
XM107 net33 net37 GND GND sky130_fd_pr__nfet_01v8 L={L} W={W} nf=1 ad='int((nf+1)/2) * W/nf * 0.29' as='int((nf+2)/2) * W/nf * 0.29'
+ pd='2*int((nf+1)/2) * (W/nf + 0.29)' ps='2*int((nf+2)/2) * (W/nf + 0.29)' nrd='0.29 / W' nrs='0.29 / W'
+ sa=0 sb=0 sd=0 mult=1 m=1
XM108 net10 net15 net34 GND sky130_fd_pr__nfet_01v8 L={L} W={W} nf=1 ad='int((nf+1)/2) * W/nf * 0.29'
+ as='int((nf+2)/2) * W/nf * 0.29' pd='2*int((nf+1)/2) * (W/nf + 0.29)' ps='2*int((nf+2)/2) * (W/nf + 0.29)'
+ nrd='0.29 / W' nrs='0.29 / W' sa=0 sb=0 sd=0 mult=1 m=1
XM109 net34 net15 net10 GND sky130_fd_pr__nfet_01v8 L={L} W={W} nf=1 ad='int((nf+1)/2) * W/nf * 0.29'
+ as='int((nf+2)/2) * W/nf * 0.29' pd='2*int((nf+1)/2) * (W/nf + 0.29)' ps='2*int((nf+2)/2) * (W/nf + 0.29)'
+ nrd='0.29 / W' nrs='0.29 / W' sa=0 sb=0 sd=0 mult=1 m=1
XM110 net30 net15 net34 GND sky130_fd_pr__nfet_01v8 L={L} W={W} nf=1 ad='int((nf+1)/2) * W/nf * 0.29'
+ as='int((nf+2)/2) * W/nf * 0.29' pd='2*int((nf+1)/2) * (W/nf + 0.29)' ps='2*int((nf+2)/2) * (W/nf + 0.29)'
+ nrd='0.29 / W' nrs='0.29 / W' sa=0 sb=0 sd=0 mult=1 m=1
XM111 net34 net15 net30 GND sky130_fd_pr__nfet_01v8 L={L} W={W} nf=1 ad='int((nf+1)/2) * W/nf * 0.29'
+ as='int((nf+2)/2) * W/nf * 0.29' pd='2*int((nf+1)/2) * (W/nf + 0.29)' ps='2*int((nf+2)/2) * (W/nf + 0.29)'
+ nrd='0.29 / W' nrs='0.29 / W' sa=0 sb=0 sd=0 mult=1 m=1
XM112 net34 b6out GND GND sky130_fd_pr__nfet_01v8 L={L} W={W} nf=1 ad='int((nf+1)/2) * W/nf * 0.29' as='int((nf+2)/2) * W/nf * 0.29'
+ pd='2*int((nf+1)/2) * (W/nf + 0.29)' ps='2*int((nf+2)/2) * (W/nf + 0.29)' nrd='0.29 / W' nrs='0.29 / W'
+ sa=0 sb=0 sd=0 mult=1 m=1
XM113 GND net38 net32 GND sky130_fd_pr__nfet_01v8 L={L} W={W} nf=1 ad='int((nf+1)/2) * W/nf * 0.29' as='int((nf+2)/2) * W/nf * 0.29'
+ pd='2*int((nf+1)/2) * (W/nf + 0.29)' ps='2*int((nf+2)/2) * (W/nf + 0.29)' nrd='0.29 / W' nrs='0.29 / W'
+ sa=0 sb=0 sd=0 mult=1 m=1
XM114 net29 net15 net32 GND sky130_fd_pr__nfet_01v8 L={L} W={W} nf=1 ad='int((nf+1)/2) * W/nf * 0.29'
+ as='int((nf+2)/2) * W/nf * 0.29' pd='2*int((nf+1)/2) * (W/nf + 0.29)' ps='2*int((nf+2)/2) * (W/nf + 0.29)'
+ nrd='0.29 / W' nrs='0.29 / W' sa=0 sb=0 sd=0 mult=1 m=1
XM115 VDD net29 net29 VDD sky130_fd_pr__pfet_01v8 L={L} W={W} nf=1 ad='int((nf+1)/2) * W/nf * 0.29' as='int((nf+2)/2) * W/nf * 0.29'
+ pd='2*int((nf+1)/2) * (W/nf + 0.29)' ps='2*int((nf+2)/2) * (W/nf + 0.29)' nrd='0.29 / W' nrs='0.29 / W'
+ sa=0 sb=0 sd=0 mult=1 m=1
Vout3 net39 GND 1.8
V7 b0 GND 1.8
V8 b1 GND 1.8
V9 b2 GND 1.8
V10 b3 GND 1.8
V11 b4 GND 1.8
V12 b5 GND 1.8
V13 b6 GND 1.8
VDD14 VDD GND 1.8
**** begin user architecture code

.param W=24
.param L=1
.dc Vout3 0 1.8 0.01
.save v(Vout3) i(Vout)


.option wnflag=1
.param MC_SWITCH=0.0
.lib ~/skywater/skywater-pdk/libraries/sky130_fd_pr_ngspice/latest/models/sky130.lib.spice tt

**** end user architecture code
**.ends

* expanding   symbol:  /home/madvlsi/Documents/current-output-dac-vlsi/schematics/mux.sym # of
*+ pins=4
** sym_path: dac/schematics/mux.sym
** sch_path: dac/schematics/mux.sch
.subckt mux A B Y S
*.ipin A
*.ipin B
*.ipin S
*.opin Y
XM1 A S Y VDD sky130_fd_pr__pfet_01v8 L=0.15 W=1 nf=1 ad='int((nf+1)/2) * W/nf * 0.29' as='int((nf+2)/2) * W/nf * 0.29'
+ pd='2*int((nf+1)/2) * (W/nf + 0.29)' ps='2*int((nf+2)/2) * (W/nf + 0.29)' nrd='0.29 / W' nrs='0.29 / W'
+ sa=0 sb=0 sd=0 mult=1 m=1
XM3 net1 S VDD VDD sky130_fd_pr__pfet_01v8 L=0.15 W=1 nf=1 ad='int((nf+1)/2) * W/nf * 0.29' as='int((nf+2)/2) * W/nf * 0.29'
+ pd='2*int((nf+1)/2) * (W/nf + 0.29)' ps='2*int((nf+2)/2) * (W/nf + 0.29)' nrd='0.29 / W' nrs='0.29 / W'
+ sa=0 sb=0 sd=0 mult=1 m=1
XM4 net1 S GND GND sky130_fd_pr__nfet_01v8 L=0.15 W=1 nf=1 ad='int((nf+1)/2) * W/nf * 0.29' as='int((nf+2)/2) * W/nf * 0.29'
+ pd='2*int((nf+1)/2) * (W/nf + 0.29)' ps='2*int((nf+2)/2) * (W/nf + 0.29)' nrd='0.29 / W' nrs='0.29 / W'
+ sa=0 sb=0 sd=0 mult=1 m=1
XM5 A net1 Y GND sky130_fd_pr__nfet_01v8 L=0.15 W=1 nf=1 ad='int((nf+1)/2) * W/nf * 0.29' as='int((nf+2)/2) * W/nf * 0.29'
+ pd='2*int((nf+1)/2) * (W/nf + 0.29)' ps='2*int((nf+2)/2) * (W/nf + 0.29)' nrd='0.29 / W' nrs='0.29 / W'
+ sa=0 sb=0 sd=0 mult=1 m=1
XM2 B net1 Y VDD sky130_fd_pr__pfet_01v8 L=0.15 W=1 nf=1 ad='int((nf+1)/2) * W/nf * 0.29' as='int((nf+2)/2) * W/nf * 0.29'
+ pd='2*int((nf+1)/2) * (W/nf + 0.29)' ps='2*int((nf+2)/2) * (W/nf + 0.29)' nrd='0.29 / W' nrs='0.29 / W'
+ sa=0 sb=0 sd=0 mult=1 m=1
XM6 B S Y GND sky130_fd_pr__nfet_01v8 L=0.15 W=1 nf=1 ad='int((nf+1)/2) * W/nf * 0.29' as='int((nf+2)/2) * W/nf * 0.29'
+ pd='2*int((nf+1)/2) * (W/nf + 0.29)' ps='2*int((nf+2)/2) * (W/nf + 0.29)' nrd='0.29 / W' nrs='0.29 / W'
+ sa=0 sb=0 sd=0 mult=1 m=1
.ends

.GLOBAL VDD
.GLOBAL GND
.end
